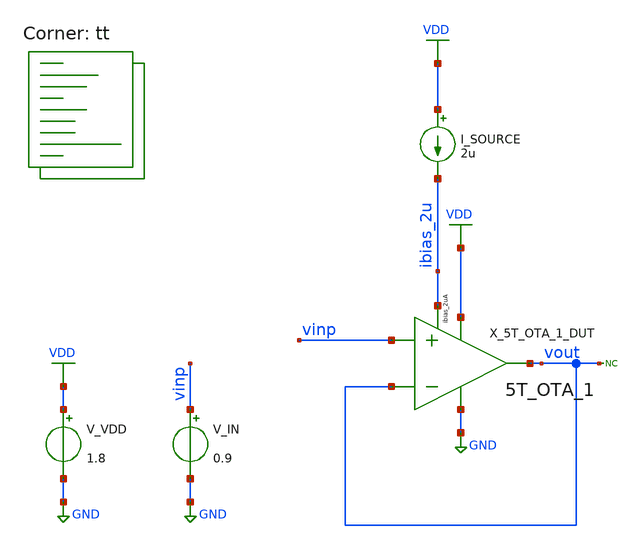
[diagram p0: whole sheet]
** sch_path: xsch/tb/tb_5T_OTA_1_DC_sweep.sch
**.subckt tb_5T_OTA_1_DC_sweep
X_5T_OTA_1_DUT vinp vout VDD GND vout ibias_2u 5T_OTA_1
V_VDD VDD GND 1.8
.save i(v_vdd)
V_IN vinp GND 0.9
.save i(v_in)
* noconn vout
I_SOURCE VDD ibias_2u 2u
**** begin user architecture code


.save v(vout) v(vinp)
.save m.x_5t_ota_1_dut.mn_in[gm]
.control
  save all

  dc V_IN 0 1.8 0.01
  *op
  plot v(vout) v(vinp)
  plot @m.x_5t_ota_1_dut.xmn_inp.msky130_fd_pr__nfet_01v8[gm]
  plot @m.x_5t_ota_1_dut.xmn_cs.msky130_fd_pr__nfet_01v8[gm]

.endc



.lib $::SKYWATER_MODELS/sky130.lib.spice tt
**** end user architecture code
**.ends
.GLOBAL VDD
.GLOBAL GND
.end
